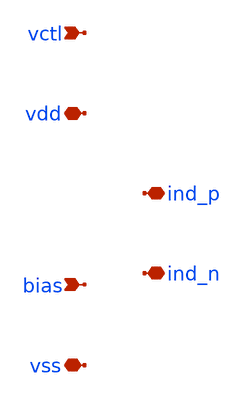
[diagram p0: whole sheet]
** sch_path: design/lc_oscillator_core/lc_oscillator_core_pex.sch
**.subckt lc_oscillator_core_pex vctl vss bias vdd ind_n ind_p
*.ipin vctl
*.iopin vss
*.ipin bias
*.iopin vdd
*.iopin ind_n
*.iopin ind_p
**** begin user architecture code



* NGSPICE file created from lc_oscillator_core.ext - technology: sky130A

.subckt sky130_fd_pr__nfet_01v8_lvt_5-00_0-15_nf8 a_351_n500# w_n439_n526# a_255_n500#  a_n413_n500#
+ a_n273_522# a_n177_n588# a_159_n500# a_n81_522# a_15_n588# a_303_522#  a_n369_n588# a_n33_n500# a_207_n588#
+ a_111_522# a_n321_n500# a_n225_n500# a_63_n500#  a_n129_n500#
X0 a_n225_n500# a_n273_522# a_n321_n500# w_n439_n526# sky130_fd_pr__nfet_01v8_lvt ad=1.65e+12p
+ pd=1.066e+07u as=1.65e+12p ps=1.066e+07u w=5e+06u l=150000u
X1 a_n129_n500# a_n177_n588# a_n225_n500# w_n439_n526# sky130_fd_pr__nfet_01v8_lvt ad=1.65e+12p
+ pd=1.066e+07u as=0p ps=0u w=5e+06u l=150000u
X2 a_n321_n500# a_n369_n588# a_n413_n500# w_n439_n526# sky130_fd_pr__nfet_01v8_lvt ad=0p pd=0u
+ as=1.55e+12p ps=1.062e+07u w=5e+06u l=150000u
X3 a_159_n500# a_111_522# a_63_n500# w_n439_n526# sky130_fd_pr__nfet_01v8_lvt ad=1.65e+12p
+ pd=1.066e+07u as=1.65e+12p ps=1.066e+07u w=5e+06u l=150000u
X4 a_255_n500# a_207_n588# a_159_n500# w_n439_n526# sky130_fd_pr__nfet_01v8_lvt ad=1.65e+12p
+ pd=1.066e+07u as=0p ps=0u w=5e+06u l=150000u
X5 a_351_n500# a_303_522# a_255_n500# w_n439_n526# sky130_fd_pr__nfet_01v8_lvt ad=1.55e+12p
+ pd=1.062e+07u as=0p ps=0u w=5e+06u l=150000u
X6 a_n33_n500# a_n81_522# a_n129_n500# w_n439_n526# sky130_fd_pr__nfet_01v8_lvt ad=1.65e+12p
+ pd=1.066e+07u as=0p ps=0u w=5e+06u l=150000u
X7 a_63_n500# a_15_n588# a_n33_n500# w_n439_n526# sky130_fd_pr__nfet_01v8_lvt ad=0p pd=0u as=0p
+ ps=0u w=5e+06u l=150000u
C0 a_n33_n500# a_63_n500# 1.44fF
C1 a_n273_522# a_111_522# 0.02fF
C2 a_n129_n500# a_255_n500# 0.23fF
C3 a_n413_n500# a_n129_n500# 0.32fF
C4 a_n321_n500# a_n225_n500# 1.44fF
C5 a_15_n588# a_n369_n588# 0.02fF
C6 a_111_522# a_303_522# 0.04fF
C7 a_n33_n500# a_159_n500# 0.52fF
C8 a_n273_522# a_n369_n588# 0.02fF
C9 a_n225_n500# a_n129_n500# 1.44fF
C10 a_n33_n500# a_255_n500# 0.32fF
C11 a_63_n500# a_159_n500# 1.44fF
C12 a_n413_n500# a_n33_n500# 0.23fF
C13 a_n225_n500# a_n33_n500# 0.52fF
C14 a_n81_522# a_111_522# 0.04fF
C15 a_n33_n500# a_351_n500# 0.23fF
C16 a_63_n500# a_255_n500# 0.52fF
C17 a_n225_n500# a_63_n500# 0.32fF
C18 a_n81_522# a_15_n588# 0.02fF
C19 a_159_n500# a_255_n500# 1.44fF
C20 a_63_n500# a_351_n500# 0.32fF
C21 a_n273_522# a_n81_522# 0.04fF
C22 a_n225_n500# a_159_n500# 0.23fF
C23 a_n177_n588# a_n369_n588# 0.04fF
C24 a_n81_522# a_303_522# 0.02fF
C25 a_n177_n588# a_15_n588# 0.04fF
C26 a_159_n500# a_351_n500# 0.52fF
C27 a_207_n588# a_111_522# 0.02fF
C28 a_n273_522# a_n177_n588# 0.02fF
C29 a_n413_n500# a_n225_n500# 0.52fF
C30 a_255_n500# a_351_n500# 1.44fF
C31 a_207_n588# a_15_n588# 0.04fF
C32 a_n321_n500# a_n129_n500# 0.52fF
C33 a_207_n588# a_303_522# 0.02fF
C34 a_n321_n500# a_n33_n500# 0.32fF
C35 a_n81_522# a_n177_n588# 0.02fF
C36 a_n129_n500# a_n33_n500# 1.44fF
C37 a_n321_n500# a_63_n500# 0.23fF
C38 a_n129_n500# a_63_n500# 0.52fF
C39 a_207_n588# a_n177_n588# 0.02fF
C40 a_n129_n500# a_159_n500# 0.32fF
C41 a_111_522# a_15_n588# 0.02fF
C42 a_n413_n500# a_n321_n500# 1.44fF
C43 a_351_n500# w_n439_n526# 0.03fF
C44 a_255_n500# w_n439_n526# 0.03fF
C45 a_159_n500# w_n439_n526# 0.03fF
C46 a_63_n500# w_n439_n526# 0.03fF
C47 a_n33_n500# w_n439_n526# 0.03fF
C48 a_n129_n500# w_n439_n526# 0.03fF
C49 a_n225_n500# w_n439_n526# 0.03fF
C50 a_n321_n500# w_n439_n526# 0.03fF
C51 a_n413_n500# w_n439_n526# 0.03fF
C52 a_207_n588# w_n439_n526# 0.12fF
C53 a_303_522# w_n439_n526# 0.12fF
C54 a_15_n588# w_n439_n526# 0.12fF
C55 a_111_522# w_n439_n526# 0.12fF
C56 a_n177_n588# w_n439_n526# 0.12fF
C57 a_n81_522# w_n439_n526# 0.12fF
C58 a_n369_n588# w_n439_n526# 0.12fF
C59 a_n273_522# w_n439_n526# 0.12fF
.ends

.subckt lc_oscillator_cascode_ sky130_fd_pr__nfet_01v8_lvt_5-00_0-15_nf8_0/a_111_522#  VSUBS
+ m1_28_951# m1_124_669# sky130_fd_pr__nfet_01v8_lvt_5-00_0-15_nf8_0/a_n369_n588#
+  sky130_fd_pr__nfet_01v8_lvt_5-00_0-15_nf8_0/a_207_n588# sky130_fd_pr__nfet_01v8_lvt_5-00_0-15_nf8_0/a_15_n588#
+  sky130_fd_pr__nfet_01v8_lvt_5-00_0-15_nf8_0/a_n81_522# sky130_fd_pr__nfet_01v8_lvt_5-00_0-15_nf8_0/a_303_522#
+  sky130_fd_pr__nfet_01v8_lvt_5-00_0-15_nf8_0/a_n273_522# sky130_fd_pr__nfet_01v8_lvt_5-00_0-15_nf8_0/a_n177_n588#
Xsky130_fd_pr__nfet_01v8_lvt_5-00_0-15_nf8_0 m1_28_951# VSUBS m1_124_669# m1_28_951#
+  sky130_fd_pr__nfet_01v8_lvt_5-00_0-15_nf8_0/a_n273_522# sky130_fd_pr__nfet_01v8_lvt_5-00_0-15_nf8_0/a_n177_n588#  m1_28_951#
+ sky130_fd_pr__nfet_01v8_lvt_5-00_0-15_nf8_0/a_n81_522# sky130_fd_pr__nfet_01v8_lvt_5-00_0-15_nf8_0/a_15_n588#
+  sky130_fd_pr__nfet_01v8_lvt_5-00_0-15_nf8_0/a_303_522# sky130_fd_pr__nfet_01v8_lvt_5-00_0-15_nf8_0/a_n369_n588#  m1_28_951#
+ sky130_fd_pr__nfet_01v8_lvt_5-00_0-15_nf8_0/a_207_n588# sky130_fd_pr__nfet_01v8_lvt_5-00_0-15_nf8_0/a_111_522#  m1_124_669# m1_28_951# m1_124_669#
+ m1_124_669# sky130_fd_pr__nfet_01v8_lvt_5-00_0-15_nf8
C0 sky130_fd_pr__nfet_01v8_lvt_5-00_0-15_nf8_0/a_n177_n588# m1_124_669# 0.05fF
C1 sky130_fd_pr__nfet_01v8_lvt_5-00_0-15_nf8_0/a_207_n588# m1_28_951# 0.05fF
C2 sky130_fd_pr__nfet_01v8_lvt_5-00_0-15_nf8_0/a_111_522# m1_124_669# 0.05fF
C3 sky130_fd_pr__nfet_01v8_lvt_5-00_0-15_nf8_0/a_15_n588# m1_124_669# 0.05fF
C4 m1_28_951# sky130_fd_pr__nfet_01v8_lvt_5-00_0-15_nf8_0/a_303_522# 0.05fF
C5 sky130_fd_pr__nfet_01v8_lvt_5-00_0-15_nf8_0/a_n273_522# m1_28_951# 0.05fF
C6 m1_28_951# m1_124_669# 4.34fF
C7 sky130_fd_pr__nfet_01v8_lvt_5-00_0-15_nf8_0/a_n369_n588# m1_28_951# 0.05fF
C8 sky130_fd_pr__nfet_01v8_lvt_5-00_0-15_nf8_0/a_207_n588# m1_124_669# 0.05fF
C9 sky130_fd_pr__nfet_01v8_lvt_5-00_0-15_nf8_0/a_n81_522# m1_28_951# 0.05fF
C10 sky130_fd_pr__nfet_01v8_lvt_5-00_0-15_nf8_0/a_n177_n588# m1_28_951# 0.05fF
C11 sky130_fd_pr__nfet_01v8_lvt_5-00_0-15_nf8_0/a_111_522# m1_28_951# 0.05fF
C12 sky130_fd_pr__nfet_01v8_lvt_5-00_0-15_nf8_0/a_303_522# m1_124_669# 0.05fF
C13 sky130_fd_pr__nfet_01v8_lvt_5-00_0-15_nf8_0/a_n273_522# m1_124_669# 0.05fF
C14 sky130_fd_pr__nfet_01v8_lvt_5-00_0-15_nf8_0/a_15_n588# m1_28_951# 0.05fF
C15 sky130_fd_pr__nfet_01v8_lvt_5-00_0-15_nf8_0/a_n369_n588# m1_124_669# 0.05fF
C16 sky130_fd_pr__nfet_01v8_lvt_5-00_0-15_nf8_0/a_n81_522# m1_124_669# 0.05fF
C17 m1_124_669# VSUBS 0.20fF
C18 m1_28_951# VSUBS 0.19fF
C19 sky130_fd_pr__nfet_01v8_lvt_5-00_0-15_nf8_0/a_207_n588# VSUBS 0.12fF
C20 sky130_fd_pr__nfet_01v8_lvt_5-00_0-15_nf8_0/a_303_522# VSUBS 0.12fF
C21 sky130_fd_pr__nfet_01v8_lvt_5-00_0-15_nf8_0/a_15_n588# VSUBS 0.12fF
C22 sky130_fd_pr__nfet_01v8_lvt_5-00_0-15_nf8_0/a_111_522# VSUBS 0.12fF
C23 sky130_fd_pr__nfet_01v8_lvt_5-00_0-15_nf8_0/a_n177_n588# VSUBS 0.12fF
C24 sky130_fd_pr__nfet_01v8_lvt_5-00_0-15_nf8_0/a_n81_522# VSUBS 0.12fF
C25 sky130_fd_pr__nfet_01v8_lvt_5-00_0-15_nf8_0/a_n369_n588# VSUBS 0.12fF
C26 sky130_fd_pr__nfet_01v8_lvt_5-00_0-15_nf8_0/a_n273_522# VSUBS 0.12fF
.ends

.subckt sky130_fd_pr__cap_mim_m3_1_6-00_6-00 VSUBS m3_n749_n700# c1_n649_n600#
X0 c1_n649_n600# m3_n749_n700# sky130_fd_pr__cap_mim_m3_1 l=6e+06u w=6e+06u
C0 c1_n649_n600# m3_n749_n700# 4.78fF
C1 m3_n749_n700# VSUBS 1.82fF
.ends

.subckt sky130_fd_pr__nfet_01v8_lvt_5-00_0-50 w_n134_n526# a_n50_n588# a_n108_n500#  a_50_n500#
X0 a_50_n500# a_n50_n588# a_n108_n500# w_n134_n526# sky130_fd_pr__nfet_01v8_lvt ad=1.45e+12p
+ pd=1.058e+07u as=1.45e+12p ps=1.058e+07u w=5e+06u l=500000u
C0 a_n108_n500# a_50_n500# 0.67fF
C1 a_50_n500# w_n134_n526# 0.03fF
C2 a_n108_n500# w_n134_n526# 0.03fF
C3 a_n50_n588# w_n134_n526# 0.21fF
.ends

.subckt lc_oscillator_current_ m1_180_574# w_n124_n146# m1_87_0# m1_180_2226#
Xsky130_fd_pr__nfet_01v8_lvt_5-00_0-50_0[0|0] w_n124_n146# m1_87_0# w_n124_n146# m1_180_574#
+  sky130_fd_pr__nfet_01v8_lvt_5-00_0-50
Xsky130_fd_pr__nfet_01v8_lvt_5-00_0-50_0[1|0] w_n124_n146# m1_87_0# w_n124_n146# m1_180_2226#
+  sky130_fd_pr__nfet_01v8_lvt_5-00_0-50
Xsky130_fd_pr__nfet_01v8_lvt_5-00_0-50_0[0|1] w_n124_n146# m1_87_0# m1_180_574# w_n124_n146#
+  sky130_fd_pr__nfet_01v8_lvt_5-00_0-50
Xsky130_fd_pr__nfet_01v8_lvt_5-00_0-50_0[1|1] w_n124_n146# m1_87_0# m1_180_2226# w_n124_n146#
+  sky130_fd_pr__nfet_01v8_lvt_5-00_0-50
Xsky130_fd_pr__nfet_01v8_lvt_5-00_0-50_0[0|2] w_n124_n146# m1_87_0# w_n124_n146# m1_180_574#
+  sky130_fd_pr__nfet_01v8_lvt_5-00_0-50
Xsky130_fd_pr__nfet_01v8_lvt_5-00_0-50_0[1|2] w_n124_n146# m1_87_0# w_n124_n146# m1_180_2226#
+  sky130_fd_pr__nfet_01v8_lvt_5-00_0-50
Xsky130_fd_pr__nfet_01v8_lvt_5-00_0-50_0[0|3] w_n124_n146# m1_87_0# m1_180_574# w_n124_n146#
+  sky130_fd_pr__nfet_01v8_lvt_5-00_0-50
Xsky130_fd_pr__nfet_01v8_lvt_5-00_0-50_0[1|3] w_n124_n146# m1_87_0# m1_180_2226# w_n124_n146#
+  sky130_fd_pr__nfet_01v8_lvt_5-00_0-50
Xsky130_fd_pr__nfet_01v8_lvt_5-00_0-50_0[0|4] w_n124_n146# m1_87_0# w_n124_n146# m1_180_574#
+  sky130_fd_pr__nfet_01v8_lvt_5-00_0-50
Xsky130_fd_pr__nfet_01v8_lvt_5-00_0-50_0[1|4] w_n124_n146# m1_87_0# w_n124_n146# m1_180_2226#
+  sky130_fd_pr__nfet_01v8_lvt_5-00_0-50
Xsky130_fd_pr__nfet_01v8_lvt_5-00_0-50_0[0|5] w_n124_n146# m1_87_0# m1_180_574# w_n124_n146#
+  sky130_fd_pr__nfet_01v8_lvt_5-00_0-50
Xsky130_fd_pr__nfet_01v8_lvt_5-00_0-50_0[1|5] w_n124_n146# m1_87_0# m1_180_2226# w_n124_n146#
+  sky130_fd_pr__nfet_01v8_lvt_5-00_0-50
Xsky130_fd_pr__nfet_01v8_lvt_5-00_0-50_0[0|6] w_n124_n146# m1_87_0# w_n124_n146# m1_180_574#
+  sky130_fd_pr__nfet_01v8_lvt_5-00_0-50
Xsky130_fd_pr__nfet_01v8_lvt_5-00_0-50_0[1|6] w_n124_n146# m1_87_0# w_n124_n146# m1_180_2226#
+  sky130_fd_pr__nfet_01v8_lvt_5-00_0-50
Xsky130_fd_pr__nfet_01v8_lvt_5-00_0-50_0[0|7] w_n124_n146# m1_87_0# m1_180_574# w_n124_n146#
+  sky130_fd_pr__nfet_01v8_lvt_5-00_0-50
Xsky130_fd_pr__nfet_01v8_lvt_5-00_0-50_0[1|7] w_n124_n146# m1_87_0# m1_180_2226# w_n124_n146#
+  sky130_fd_pr__nfet_01v8_lvt_5-00_0-50
Xsky130_fd_pr__nfet_01v8_lvt_5-00_0-50_0[0|8] w_n124_n146# m1_87_0# w_n124_n146# m1_180_574#
+  sky130_fd_pr__nfet_01v8_lvt_5-00_0-50
Xsky130_fd_pr__nfet_01v8_lvt_5-00_0-50_0[1|8] w_n124_n146# m1_87_0# w_n124_n146# m1_180_2226#
+  sky130_fd_pr__nfet_01v8_lvt_5-00_0-50
Xsky130_fd_pr__nfet_01v8_lvt_5-00_0-50_0[0|9] w_n124_n146# m1_87_0# m1_180_574# w_n124_n146#
+  sky130_fd_pr__nfet_01v8_lvt_5-00_0-50
Xsky130_fd_pr__nfet_01v8_lvt_5-00_0-50_0[1|9] w_n124_n146# m1_87_0# m1_180_2226# w_n124_n146#
+  sky130_fd_pr__nfet_01v8_lvt_5-00_0-50
Xsky130_fd_pr__nfet_01v8_lvt_5-00_0-50_0[0|10] w_n124_n146# m1_87_0# w_n124_n146#  m1_180_574#
+ sky130_fd_pr__nfet_01v8_lvt_5-00_0-50
Xsky130_fd_pr__nfet_01v8_lvt_5-00_0-50_0[1|10] w_n124_n146# m1_87_0# w_n124_n146#  m1_180_2226#
+ sky130_fd_pr__nfet_01v8_lvt_5-00_0-50
Xsky130_fd_pr__nfet_01v8_lvt_5-00_0-50_0[0|11] w_n124_n146# m1_87_0# m1_180_574# w_n124_n146#
+  sky130_fd_pr__nfet_01v8_lvt_5-00_0-50
Xsky130_fd_pr__nfet_01v8_lvt_5-00_0-50_0[1|11] w_n124_n146# m1_87_0# m1_180_2226#  w_n124_n146#
+ sky130_fd_pr__nfet_01v8_lvt_5-00_0-50
Xsky130_fd_pr__nfet_01v8_lvt_5-00_0-50_0[0|12] w_n124_n146# m1_87_0# w_n124_n146#  m1_180_574#
+ sky130_fd_pr__nfet_01v8_lvt_5-00_0-50
Xsky130_fd_pr__nfet_01v8_lvt_5-00_0-50_0[1|12] w_n124_n146# m1_87_0# w_n124_n146#  m1_180_2226#
+ sky130_fd_pr__nfet_01v8_lvt_5-00_0-50
Xsky130_fd_pr__nfet_01v8_lvt_5-00_0-50_0[0|13] w_n124_n146# m1_87_0# m1_180_574# w_n124_n146#
+  sky130_fd_pr__nfet_01v8_lvt_5-00_0-50
Xsky130_fd_pr__nfet_01v8_lvt_5-00_0-50_0[1|13] w_n124_n146# m1_87_0# m1_180_2226#  w_n124_n146#
+ sky130_fd_pr__nfet_01v8_lvt_5-00_0-50
Xsky130_fd_pr__nfet_01v8_lvt_5-00_0-50_0[0|14] w_n124_n146# m1_87_0# w_n124_n146#  m1_180_574#
+ sky130_fd_pr__nfet_01v8_lvt_5-00_0-50
Xsky130_fd_pr__nfet_01v8_lvt_5-00_0-50_0[1|14] w_n124_n146# m1_87_0# w_n124_n146#  m1_180_2226#
+ sky130_fd_pr__nfet_01v8_lvt_5-00_0-50
Xsky130_fd_pr__nfet_01v8_lvt_5-00_0-50_0[0|15] w_n124_n146# m1_87_0# m1_180_574# w_n124_n146#
+  sky130_fd_pr__nfet_01v8_lvt_5-00_0-50
Xsky130_fd_pr__nfet_01v8_lvt_5-00_0-50_0[1|15] w_n124_n146# m1_87_0# m1_180_2226#  w_n124_n146#
+ sky130_fd_pr__nfet_01v8_lvt_5-00_0-50
Xsky130_fd_pr__nfet_01v8_lvt_5-00_0-50_0[0|16] w_n124_n146# m1_87_0# w_n124_n146#  m1_87_0#
+ sky130_fd_pr__nfet_01v8_lvt_5-00_0-50
Xsky130_fd_pr__nfet_01v8_lvt_5-00_0-50_0[1|16] w_n124_n146# m1_87_0# w_n124_n146#  m1_180_2226#
+ sky130_fd_pr__nfet_01v8_lvt_5-00_0-50
Xsky130_fd_pr__nfet_01v8_lvt_5-00_0-50_0[0|17] w_n124_n146# m1_87_0# m1_87_0# w_n124_n146#
+  sky130_fd_pr__nfet_01v8_lvt_5-00_0-50
Xsky130_fd_pr__nfet_01v8_lvt_5-00_0-50_0[1|17] w_n124_n146# m1_87_0# m1_180_2226#  w_n124_n146#
+ sky130_fd_pr__nfet_01v8_lvt_5-00_0-50
Xsky130_fd_pr__nfet_01v8_lvt_5-00_0-50_0[0|18] w_n124_n146# m1_87_0# w_n124_n146#  m1_180_574#
+ sky130_fd_pr__nfet_01v8_lvt_5-00_0-50
Xsky130_fd_pr__nfet_01v8_lvt_5-00_0-50_0[1|18] w_n124_n146# m1_87_0# w_n124_n146#  m1_180_2226#
+ sky130_fd_pr__nfet_01v8_lvt_5-00_0-50
Xsky130_fd_pr__nfet_01v8_lvt_5-00_0-50_0[0|19] w_n124_n146# m1_87_0# m1_180_574# w_n124_n146#
+  sky130_fd_pr__nfet_01v8_lvt_5-00_0-50
Xsky130_fd_pr__nfet_01v8_lvt_5-00_0-50_0[1|19] w_n124_n146# m1_87_0# m1_180_2226#  w_n124_n146#
+ sky130_fd_pr__nfet_01v8_lvt_5-00_0-50
Xsky130_fd_pr__nfet_01v8_lvt_5-00_0-50_0[0|20] w_n124_n146# m1_87_0# w_n124_n146#  m1_180_574#
+ sky130_fd_pr__nfet_01v8_lvt_5-00_0-50
Xsky130_fd_pr__nfet_01v8_lvt_5-00_0-50_0[1|20] w_n124_n146# m1_87_0# w_n124_n146#  m1_180_2226#
+ sky130_fd_pr__nfet_01v8_lvt_5-00_0-50
Xsky130_fd_pr__nfet_01v8_lvt_5-00_0-50_0[0|21] w_n124_n146# m1_87_0# m1_180_574# w_n124_n146#
+  sky130_fd_pr__nfet_01v8_lvt_5-00_0-50
Xsky130_fd_pr__nfet_01v8_lvt_5-00_0-50_0[1|21] w_n124_n146# m1_87_0# m1_180_2226#  w_n124_n146#
+ sky130_fd_pr__nfet_01v8_lvt_5-00_0-50
Xsky130_fd_pr__nfet_01v8_lvt_5-00_0-50_0[0|22] w_n124_n146# m1_87_0# w_n124_n146#  m1_180_574#
+ sky130_fd_pr__nfet_01v8_lvt_5-00_0-50
Xsky130_fd_pr__nfet_01v8_lvt_5-00_0-50_0[1|22] w_n124_n146# m1_87_0# w_n124_n146#  m1_180_2226#
+ sky130_fd_pr__nfet_01v8_lvt_5-00_0-50
Xsky130_fd_pr__nfet_01v8_lvt_5-00_0-50_0[0|23] w_n124_n146# m1_87_0# m1_180_574# w_n124_n146#
+  sky130_fd_pr__nfet_01v8_lvt_5-00_0-50
Xsky130_fd_pr__nfet_01v8_lvt_5-00_0-50_0[1|23] w_n124_n146# m1_87_0# m1_180_2226#  w_n124_n146#
+ sky130_fd_pr__nfet_01v8_lvt_5-00_0-50
Xsky130_fd_pr__nfet_01v8_lvt_5-00_0-50_0[0|24] w_n124_n146# m1_87_0# w_n124_n146#  m1_180_574#
+ sky130_fd_pr__nfet_01v8_lvt_5-00_0-50
Xsky130_fd_pr__nfet_01v8_lvt_5-00_0-50_0[1|24] w_n124_n146# m1_87_0# w_n124_n146#  m1_180_2226#
+ sky130_fd_pr__nfet_01v8_lvt_5-00_0-50
Xsky130_fd_pr__nfet_01v8_lvt_5-00_0-50_0[0|25] w_n124_n146# m1_87_0# m1_180_574# w_n124_n146#
+  sky130_fd_pr__nfet_01v8_lvt_5-00_0-50
Xsky130_fd_pr__nfet_01v8_lvt_5-00_0-50_0[1|25] w_n124_n146# m1_87_0# m1_180_2226#  w_n124_n146#
+ sky130_fd_pr__nfet_01v8_lvt_5-00_0-50
Xsky130_fd_pr__nfet_01v8_lvt_5-00_0-50_0[0|26] w_n124_n146# m1_87_0# w_n124_n146#  m1_180_574#
+ sky130_fd_pr__nfet_01v8_lvt_5-00_0-50
Xsky130_fd_pr__nfet_01v8_lvt_5-00_0-50_0[1|26] w_n124_n146# m1_87_0# w_n124_n146#  m1_180_2226#
+ sky130_fd_pr__nfet_01v8_lvt_5-00_0-50
Xsky130_fd_pr__nfet_01v8_lvt_5-00_0-50_0[0|27] w_n124_n146# m1_87_0# m1_180_574# w_n124_n146#
+  sky130_fd_pr__nfet_01v8_lvt_5-00_0-50
Xsky130_fd_pr__nfet_01v8_lvt_5-00_0-50_0[1|27] w_n124_n146# m1_87_0# m1_180_2226#  w_n124_n146#
+ sky130_fd_pr__nfet_01v8_lvt_5-00_0-50
Xsky130_fd_pr__nfet_01v8_lvt_5-00_0-50_0[0|28] w_n124_n146# m1_87_0# w_n124_n146#  m1_180_574#
+ sky130_fd_pr__nfet_01v8_lvt_5-00_0-50
Xsky130_fd_pr__nfet_01v8_lvt_5-00_0-50_0[1|28] w_n124_n146# m1_87_0# w_n124_n146#  m1_180_2226#
+ sky130_fd_pr__nfet_01v8_lvt_5-00_0-50
Xsky130_fd_pr__nfet_01v8_lvt_5-00_0-50_0[0|29] w_n124_n146# m1_87_0# m1_180_574# w_n124_n146#
+  sky130_fd_pr__nfet_01v8_lvt_5-00_0-50
Xsky130_fd_pr__nfet_01v8_lvt_5-00_0-50_0[1|29] w_n124_n146# m1_87_0# m1_180_2226#  w_n124_n146#
+ sky130_fd_pr__nfet_01v8_lvt_5-00_0-50
Xsky130_fd_pr__nfet_01v8_lvt_5-00_0-50_0[0|30] w_n124_n146# m1_87_0# w_n124_n146#  m1_180_574#
+ sky130_fd_pr__nfet_01v8_lvt_5-00_0-50
Xsky130_fd_pr__nfet_01v8_lvt_5-00_0-50_0[1|30] w_n124_n146# m1_87_0# w_n124_n146#  m1_180_2226#
+ sky130_fd_pr__nfet_01v8_lvt_5-00_0-50
Xsky130_fd_pr__nfet_01v8_lvt_5-00_0-50_0[0|31] w_n124_n146# m1_87_0# m1_180_574# w_n124_n146#
+  sky130_fd_pr__nfet_01v8_lvt_5-00_0-50
Xsky130_fd_pr__nfet_01v8_lvt_5-00_0-50_0[1|31] w_n124_n146# m1_87_0# m1_180_2226#  w_n124_n146#
+ sky130_fd_pr__nfet_01v8_lvt_5-00_0-50
Xsky130_fd_pr__nfet_01v8_lvt_5-00_0-50_0[0|32] w_n124_n146# m1_87_0# w_n124_n146#  m1_180_574#
+ sky130_fd_pr__nfet_01v8_lvt_5-00_0-50
Xsky130_fd_pr__nfet_01v8_lvt_5-00_0-50_0[1|32] w_n124_n146# m1_87_0# w_n124_n146#  m1_180_2226#
+ sky130_fd_pr__nfet_01v8_lvt_5-00_0-50
C0 m1_180_2226# m1_180_574# 1.28fF
C1 m1_180_2226# m1_87_0# 6.92fF
C2 m1_180_574# m1_87_0# 9.44fF
C3 m1_87_0# w_n124_n146# 31.92fF
C4 m1_180_574# w_n124_n146# 26.95fF
C5 m1_180_2226# w_n124_n146# 28.68fF
.ends

.subckt lc_oscillator_xcoupled_ sky130_fd_pr__nfet_01v8_lvt_5-00_0-15_nf8_0/a_111_522#  VSUBS
+ sky130_fd_pr__nfet_01v8_lvt_5-00_0-15_nf8_0/a_n369_n588# sky130_fd_pr__nfet_01v8_lvt_5-00_0-15_nf8_0/a_207_n588#  m1_124_669# m1_28_951#
+ sky130_fd_pr__nfet_01v8_lvt_5-00_0-15_nf8_0/a_15_n588# sky130_fd_pr__nfet_01v8_lvt_5-00_0-15_nf8_0/a_n81_522#
+  sky130_fd_pr__nfet_01v8_lvt_5-00_0-15_nf8_0/a_303_522# sky130_fd_pr__nfet_01v8_lvt_5-00_0-15_nf8_0/a_n273_522#
+  sky130_fd_pr__nfet_01v8_lvt_5-00_0-15_nf8_0/a_n177_n588#
Xsky130_fd_pr__nfet_01v8_lvt_5-00_0-15_nf8_0 m1_28_951# VSUBS m1_124_669# m1_28_951#
+  sky130_fd_pr__nfet_01v8_lvt_5-00_0-15_nf8_0/a_n273_522# sky130_fd_pr__nfet_01v8_lvt_5-00_0-15_nf8_0/a_n177_n588#  m1_28_951#
+ sky130_fd_pr__nfet_01v8_lvt_5-00_0-15_nf8_0/a_n81_522# sky130_fd_pr__nfet_01v8_lvt_5-00_0-15_nf8_0/a_15_n588#
+  sky130_fd_pr__nfet_01v8_lvt_5-00_0-15_nf8_0/a_303_522# sky130_fd_pr__nfet_01v8_lvt_5-00_0-15_nf8_0/a_n369_n588#  m1_28_951#
+ sky130_fd_pr__nfet_01v8_lvt_5-00_0-15_nf8_0/a_207_n588# sky130_fd_pr__nfet_01v8_lvt_5-00_0-15_nf8_0/a_111_522#  m1_124_669# m1_28_951# m1_124_669#
+ m1_124_669# sky130_fd_pr__nfet_01v8_lvt_5-00_0-15_nf8
C0 m1_28_951# sky130_fd_pr__nfet_01v8_lvt_5-00_0-15_nf8_0/a_303_522# 0.05fF
C1 sky130_fd_pr__nfet_01v8_lvt_5-00_0-15_nf8_0/a_111_522# m1_124_669# 0.05fF
C2 m1_124_669# sky130_fd_pr__nfet_01v8_lvt_5-00_0-15_nf8_0/a_303_522# 0.05fF
C3 m1_124_669# m1_28_951# 4.00fF
C4 sky130_fd_pr__nfet_01v8_lvt_5-00_0-15_nf8_0/a_n273_522# m1_28_951# 0.05fF
C5 sky130_fd_pr__nfet_01v8_lvt_5-00_0-15_nf8_0/a_n273_522# m1_124_669# 0.05fF
C6 m1_28_951# sky130_fd_pr__nfet_01v8_lvt_5-00_0-15_nf8_0/a_n177_n588# 0.05fF
C7 m1_124_669# sky130_fd_pr__nfet_01v8_lvt_5-00_0-15_nf8_0/a_n177_n588# 0.05fF
C8 m1_28_951# sky130_fd_pr__nfet_01v8_lvt_5-00_0-15_nf8_0/a_207_n588# 0.05fF
C9 m1_28_951# sky130_fd_pr__nfet_01v8_lvt_5-00_0-15_nf8_0/a_n369_n588# 0.05fF
C10 m1_124_669# sky130_fd_pr__nfet_01v8_lvt_5-00_0-15_nf8_0/a_207_n588# 0.05fF
C11 m1_124_669# sky130_fd_pr__nfet_01v8_lvt_5-00_0-15_nf8_0/a_n369_n588# 0.05fF
C12 sky130_fd_pr__nfet_01v8_lvt_5-00_0-15_nf8_0/a_n81_522# m1_28_951# 0.05fF
C13 sky130_fd_pr__nfet_01v8_lvt_5-00_0-15_nf8_0/a_n81_522# m1_124_669# 0.05fF
C14 m1_28_951# sky130_fd_pr__nfet_01v8_lvt_5-00_0-15_nf8_0/a_15_n588# 0.05fF
C15 m1_124_669# sky130_fd_pr__nfet_01v8_lvt_5-00_0-15_nf8_0/a_15_n588# 0.05fF
C16 sky130_fd_pr__nfet_01v8_lvt_5-00_0-15_nf8_0/a_111_522# m1_28_951# 0.05fF
C17 m1_124_669# VSUBS 0.42fF
C18 m1_28_951# VSUBS 0.29fF
C19 sky130_fd_pr__nfet_01v8_lvt_5-00_0-15_nf8_0/a_207_n588# VSUBS 0.12fF
C20 sky130_fd_pr__nfet_01v8_lvt_5-00_0-15_nf8_0/a_303_522# VSUBS 0.12fF
C21 sky130_fd_pr__nfet_01v8_lvt_5-00_0-15_nf8_0/a_15_n588# VSUBS 0.12fF
C22 sky130_fd_pr__nfet_01v8_lvt_5-00_0-15_nf8_0/a_111_522# VSUBS 0.12fF
C23 sky130_fd_pr__nfet_01v8_lvt_5-00_0-15_nf8_0/a_n177_n588# VSUBS 0.12fF
C24 sky130_fd_pr__nfet_01v8_lvt_5-00_0-15_nf8_0/a_n81_522# VSUBS 0.12fF
C25 sky130_fd_pr__nfet_01v8_lvt_5-00_0-15_nf8_0/a_n369_n588# VSUBS 0.12fF
C26 sky130_fd_pr__nfet_01v8_lvt_5-00_0-15_nf8_0/a_n273_522# VSUBS 0.12fF
.ends

.subckt lc_oscillator_lower_ m1_1219_1162# m1_447_174# m3_1224_880# lc_oscillator_xcoupled__1/VSUBS
Xlc_oscillator_xcoupled__0 m1_1219_1162# lc_oscillator_xcoupled__1/VSUBS m1_1219_1162#
+  m1_1219_1162# m3_1224_880# m1_447_174# m1_1219_1162# m1_1219_1162# m1_1219_1162#  m1_1219_1162# m1_1219_1162#
+ lc_oscillator_xcoupled_
Xlc_oscillator_xcoupled__1 m1_447_174# lc_oscillator_xcoupled__1/VSUBS m1_447_174#  m1_447_174#
+ m3_1224_880# m1_1219_1162# m1_447_174# m1_447_174# m1_447_174# m1_447_174#  m1_447_174# lc_oscillator_xcoupled_
C0 m1_1219_1162# m3_1224_880# 1.03fF
C1 m1_447_174# m1_1219_1162# 2.83fF
C2 m1_447_174# m3_1224_880# 0.78fF
C3 m1_1219_1162# lc_oscillator_xcoupled__1/VSUBS 4.40fF
C4 m3_1224_880# lc_oscillator_xcoupled__1/VSUBS 0.88fF
C5 m1_447_174# lc_oscillator_xcoupled__1/VSUBS 3.40fF
.ends

.subckt sky130_fd_pr__pfet_01v8_4-00_4-00 VSUBS a_n458_n400# w_n494_n500# a_400_n400#  a_n400_n497#
X0 a_400_n400# a_n400_n497# a_n458_n400# w_n494_n500# sky130_fd_pr__pfet_01v8 ad=1.16e+12p
+ pd=8.58e+06u as=1.16e+12p ps=8.58e+06u w=4e+06u l=4e+06u
C0 a_400_n400# VSUBS 0.03fF
C1 a_n458_n400# VSUBS 0.03fF
C2 a_n400_n497# VSUBS 0.97fF
C3 w_n494_n500# VSUBS 2.96fF
.ends

.subckt lc_oscillator_varactor_ VSUBS contact$37_2/m1_n26_n384# contact$37_3/m1_n26_n384#  w_0_0#
Xsky130_fd_pr__pfet_01v8_4-00_4-00_0[0] VSUBS w_0_0# w_0_0# w_0_0# contact$37_3/m1_n26_n384#
+  sky130_fd_pr__pfet_01v8_4-00_4-00
Xsky130_fd_pr__pfet_01v8_4-00_4-00_0[1] VSUBS w_0_0# w_0_0# w_0_0# contact$37_2/m1_n26_n384#
+  sky130_fd_pr__pfet_01v8_4-00_4-00
C0 w_0_0# contact$37_3/m1_n26_n384# 0.86fF
C1 contact$37_3/m1_n26_n384# contact$37_2/m1_n26_n384# 0.28fF
C2 w_0_0# contact$37_2/m1_n26_n384# 0.90fF
C3 w_0_0# VSUBS 14.15fF
C4 contact$37_3/m1_n26_n384# VSUBS 2.36fF
C5 contact$37_2/m1_n26_n384# VSUBS 2.36fF
.ends


* Top level circuit lc_oscillator_core

Xlc_oscillator_cascode__0 vdd vss ind_p m4_n71_3164# vdd vdd vdd vdd vdd vdd vdd
+ lc_oscillator_cascode_
Xsky130_fd_pr__cap_mim_m3_1_6-00_6-00_7 vss m4_n71_3164# ind_p sky130_fd_pr__cap_mim_m3_1_6-00_6-00
Xlc_oscillator_cascode__1 vdd vss ind_n m4_4623_6058# vdd vdd vdd vdd vdd vdd vdd
+  lc_oscillator_cascode_
Xsky130_fd_pr__cap_mim_m3_1_6-00_6-00_8 vss sky130_fd_pr__cap_mim_m3_1_6-00_6-00_9/m3_n749_n700#
+  m4_4623_6058# sky130_fd_pr__cap_mim_m3_1_6-00_6-00
Xsky130_fd_pr__cap_mim_m3_1_6-00_6-00_9 vss sky130_fd_pr__cap_mim_m3_1_6-00_6-00_9/m3_n749_n700#
+  m4_n71_3164# sky130_fd_pr__cap_mim_m3_1_6-00_6-00
Xlc_oscillator_current__0 m2_n89_n2022# vss bias m2_n89_n2022# lc_oscillator_current_
Xlc_oscillator_lower__0 m4_n71_3164# m4_4623_6058# m2_n89_n2022# vss lc_oscillator_lower_
Xlc_oscillator_varactor__0 vss ind_n ind_p vctl lc_oscillator_varactor_
Xsky130_fd_pr__cap_mim_m3_1_6-00_6-00_0 vss m4_4623_6058# ind_n sky130_fd_pr__cap_mim_m3_1_6-00_6-00
Xsky130_fd_pr__cap_mim_m3_1_6-00_6-00_1 vss m4_4623_6058# ind_n sky130_fd_pr__cap_mim_m3_1_6-00_6-00
Xsky130_fd_pr__cap_mim_m3_1_6-00_6-00_2 vss m4_4623_6058# ind_n sky130_fd_pr__cap_mim_m3_1_6-00_6-00
Xsky130_fd_pr__cap_mim_m3_1_6-00_6-00_3 vss m4_4623_6058# ind_n sky130_fd_pr__cap_mim_m3_1_6-00_6-00
Xsky130_fd_pr__cap_mim_m3_1_6-00_6-00_4 vss m4_n71_3164# ind_p sky130_fd_pr__cap_mim_m3_1_6-00_6-00
Xsky130_fd_pr__cap_mim_m3_1_6-00_6-00_5 vss m4_n71_3164# ind_p sky130_fd_pr__cap_mim_m3_1_6-00_6-00
Xsky130_fd_pr__cap_mim_m3_1_6-00_6-00_6 vss m4_n71_3164# ind_p sky130_fd_pr__cap_mim_m3_1_6-00_6-00
C0 m4_4623_6058# vdd 0.60fF
C1 ind_p li_562_3678# 0.95fF
C2 m4_n71_3164# ind_n 0.28fF
C3 m4_4623_6058# m4_n71_3164# 1.28fF
C4 m4_4623_6058# ind_n 1.02fF
C5 vdd ind_p 1.04fF
C6 ind_p m4_n71_3164# 2.80fF
C7 ind_p ind_n 1.15fF
C8 vctl li_562_3678# 1.00fF
C9 m4_4623_6058# ind_p 0.28fF
C10 m2_n89_n2022# m4_n71_3164# 1.30fF
C11 vdd vctl 0.57fF
C12 m2_n89_n2022# m4_4623_6058# 0.68fF
C13 vctl m4_n71_3164# 0.04fF
C14 vctl ind_n 4.06fF
C15 m4_4623_6058# vctl 0.04fF
C16 vctl ind_p 2.05fF
C17 sky130_fd_pr__cap_mim_m3_1_6-00_6-00_9/m3_n749_n700# m4_n71_3164# 0.89fF
C18 sky130_fd_pr__cap_mim_m3_1_6-00_6-00_9/m3_n749_n700# m4_4623_6058# 0.15fF
C19 vdd li_562_3678# 0.37fF
C20 m4_n71_3164# li_562_3678# 0.51fF
C21 ind_n li_562_3678# 0.95fF
C22 m4_4623_6058# li_562_3678# 0.51fF
C23 vdd m4_n71_3164# 0.60fF
C24 vdd ind_n 1.04fF
C25 m2_n89_n2022# bias 0.87fF
C26 li_562_3678# vss 4.01fF $ **FLOATING
C27 vctl vss 15.43fF
C28 m4_n71_3164# vss 1.05fF
C29 m4_4623_6058# vss 7.41fF
C30 bias vss 20.21fF
C31 m2_n89_n2022# vss 18.76fF
C32 sky130_fd_pr__cap_mim_m3_1_6-00_6-00_9/m3_n749_n700# vss 4.52fF
C33 ind_n vss 5.55fF
C34 vdd vss 3.14fF
C35 ind_p vss 0.75fF
.end




**** end user architecture code
**.ends
.end
